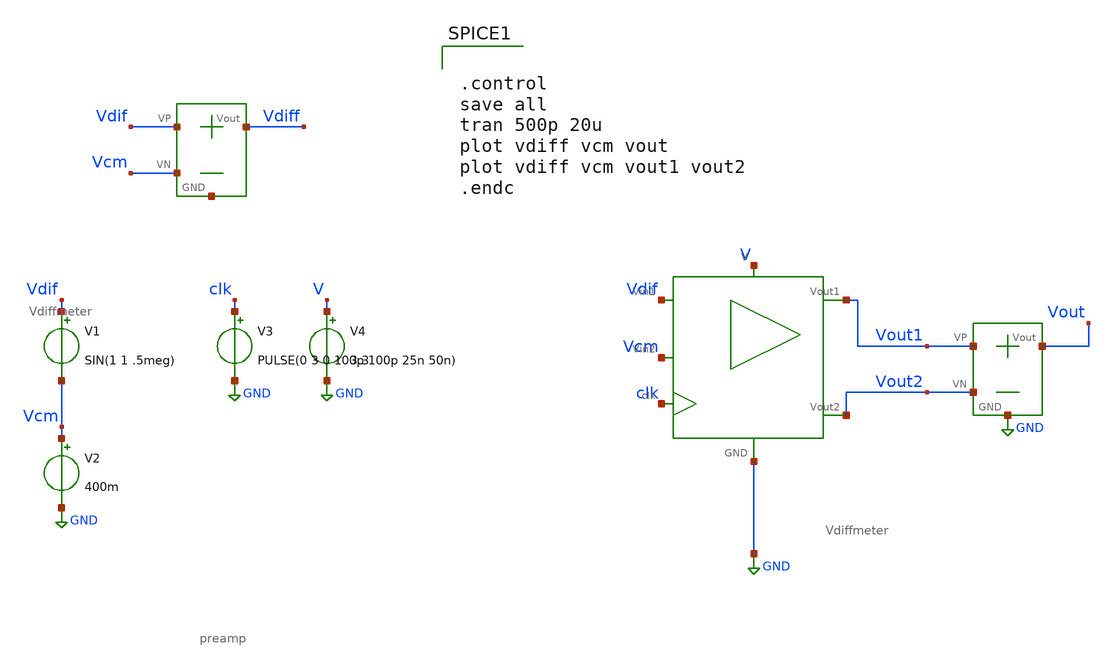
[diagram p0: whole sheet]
** sch_path: SAR_ADC/xschem/test/preamp_tb/vdif_sin-vcm_grounded__tb.sch
**.subckt vdif_sin-vcm_grounded__tb
V1 Vdif Vcm SIN(1 1 .5meg)
V3 clk GND PULSE(0 3 0 100p 100p 25n 50n)
V4 V GND 3.3
X1 V GND Vdif clk Vout1 Vout2 Vcm preamp
X3 Vout1 Vout2 Vout GND Vdiffmeter
X2 Vdif Vcm Vdiff net1 Vdiffmeter
V2 Vcm GND 400m
**** begin user architecture code


.control
save all
tran 500p 20u
plot vdiff vcm vout
plot vdiff vcm vout1 vout2
.endc


.include /foss/pdks/gf180mcuC/libs.tech/ngspice/design.ngspice
.lib /foss/pdks/gf180mcuC/libs.tech/ngspice/sm141064.ngspice typical

**** end user architecture code
**.ends
.GLOBAL GND
.end
